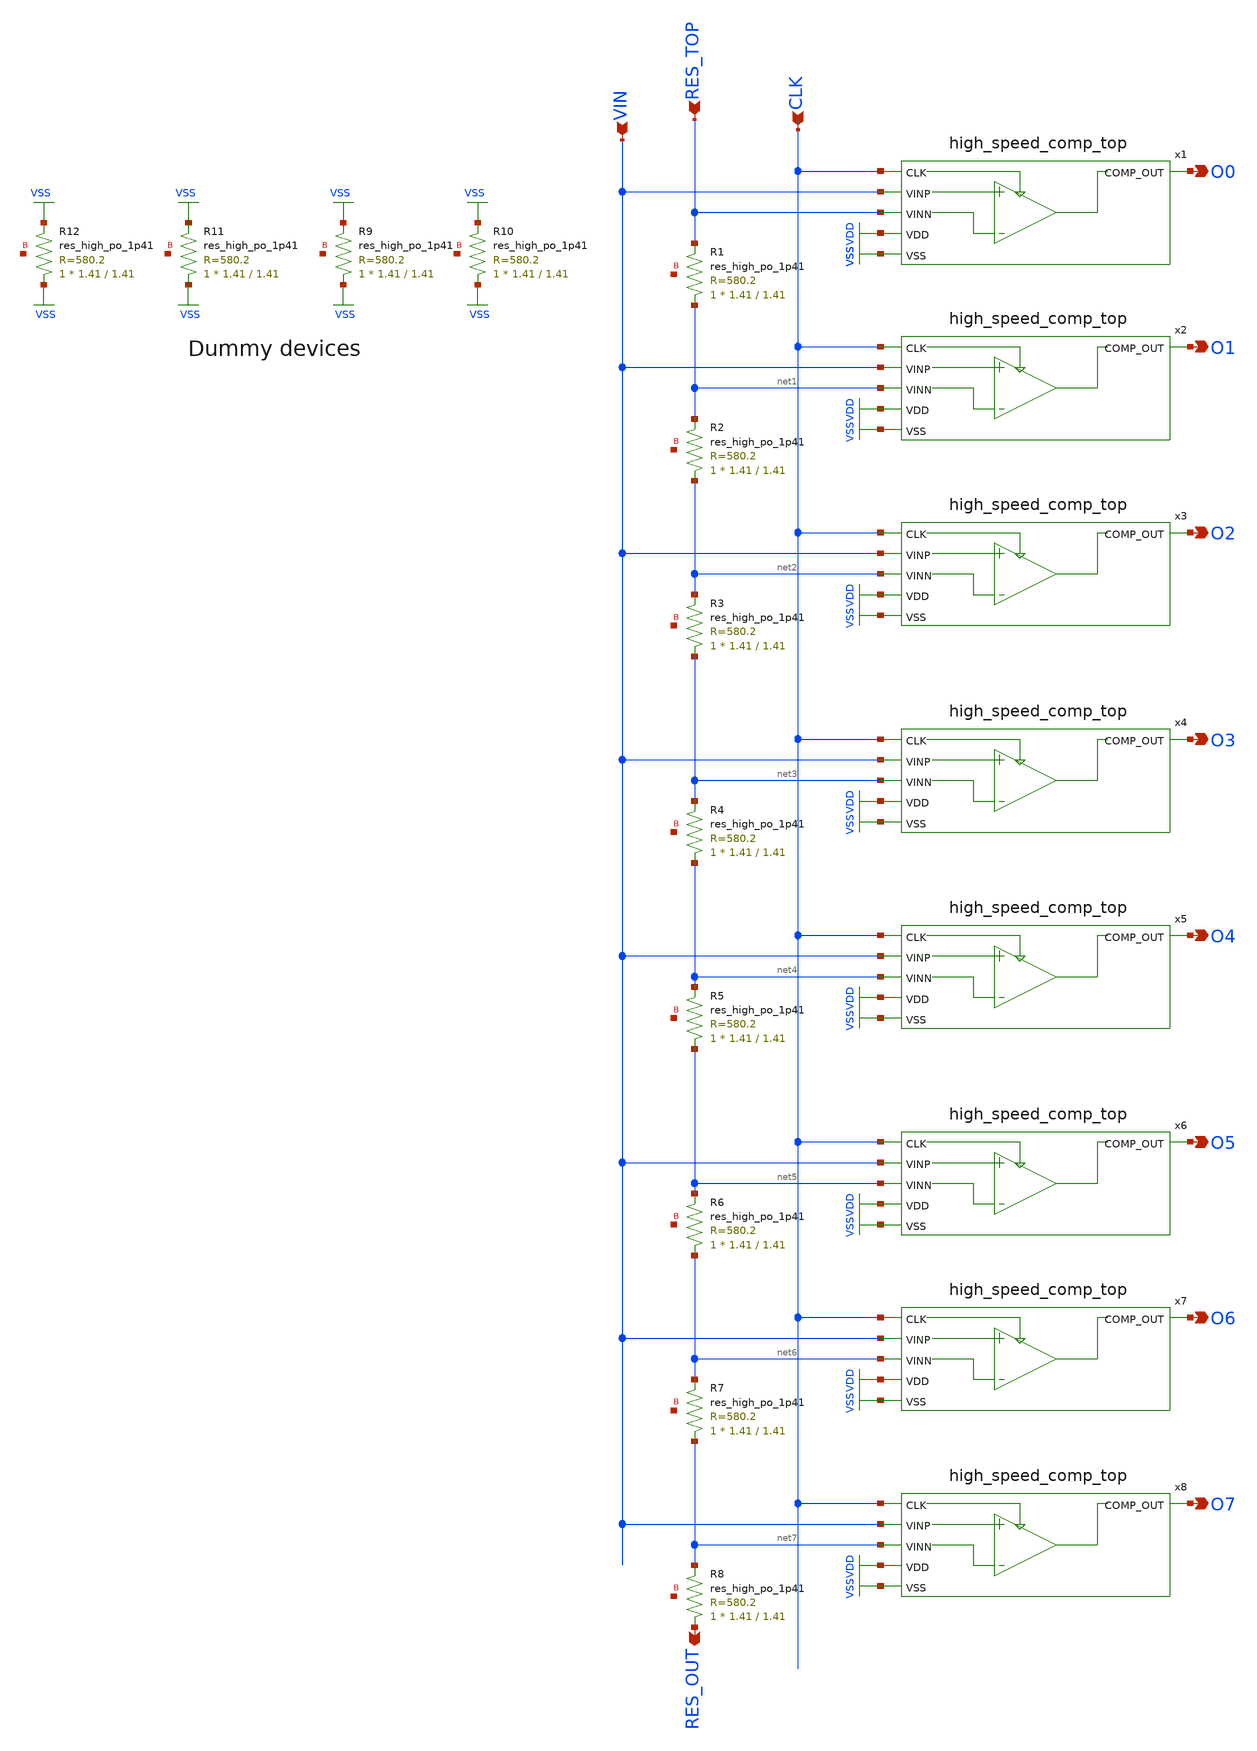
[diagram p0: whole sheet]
** sch_path: xschem/flash_converter/flash_converter.sch
**.subckt flash_converter VIN RES_TOP RES_OUT O0 O1 O2 O3 O4 O5 O6 O7 CLK
*.ipin VIN
*.ipin RES_TOP
*.opin RES_OUT
*.opin O0
*.opin O1
*.opin O2
*.opin O3
*.opin O4
*.opin O5
*.opin O6
*.opin O7
*.ipin CLK
x1 CLK VIN RES_TOP VDD O0 VSS high_speed_comp_top
x2 CLK VIN net1 VDD O1 VSS high_speed_comp_top
x3 CLK VIN net2 VDD O2 VSS high_speed_comp_top
x4 CLK VIN net3 VDD O3 VSS high_speed_comp_top
x5 CLK VIN net4 VDD O4 VSS high_speed_comp_top
x6 CLK VIN net5 VDD O5 VSS high_speed_comp_top
x7 CLK VIN net6 VDD O6 VSS high_speed_comp_top
x8 CLK VIN net7 VDD O7 VSS high_speed_comp_top
XR1 net1 RES_TOP net8 sky130_fd_pr__res_high_po_1p41 L=1.41 mult=1 m=1
XR2 net2 net1 net9 sky130_fd_pr__res_high_po_1p41 L=1.41 mult=1 m=1
XR3 net3 net2 net10 sky130_fd_pr__res_high_po_1p41 L=1.41 mult=1 m=1
XR4 net4 net3 net11 sky130_fd_pr__res_high_po_1p41 L=1.41 mult=1 m=1
XR5 net5 net4 net12 sky130_fd_pr__res_high_po_1p41 L=1.41 mult=1 m=1
XR6 net6 net5 net13 sky130_fd_pr__res_high_po_1p41 L=1.41 mult=1 m=1
XR7 net7 net6 net14 sky130_fd_pr__res_high_po_1p41 L=1.41 mult=1 m=1
XR8 RES_OUT net7 net15 sky130_fd_pr__res_high_po_1p41 L=1.41 mult=1 m=1
XR9 VSS VSS net16 sky130_fd_pr__res_high_po_1p41 L=1.41 mult=1 m=1
XR10 VSS VSS net17 sky130_fd_pr__res_high_po_1p41 L=1.41 mult=1 m=1
XR11 VSS VSS net18 sky130_fd_pr__res_high_po_1p41 L=1.41 mult=1 m=1
XR12 VSS VSS net19 sky130_fd_pr__res_high_po_1p41 L=1.41 mult=1 m=1
**.ends

* expanding   symbol:  high_speed_comp_top.sym # of pins=6
** sym_path: xschem/flash_converter/high_speed_comp_top.sym
** sch_path: xschem/flash_converter/high_speed_comp_top.sch
.subckt high_speed_comp_top CLK VINP VINN VDD COMP_OUT VSS
*.ipin VINP
*.ipin VINN
*.ipin CLK
*.opin COMP_OUT
*.ipin VDD
*.ipin VSS
x1 VDD CLK_PRIME net1 net2 VSS VINP VINN strong_arm_latch
x2 VDD net1 net2 VOUT VSS post_amplifier
x3 CLK VOUT VSS VSS VDD VDD COMP_OUT sky130_fd_sc_hd__dfxtp_2
x4 CLK VSS VSS VDD VDD CLK_PRIME sky130_fd_sc_hd__clkinv_4
x5 VSS VSS VDD VDD sky130_fd_sc_hd__decap_3
x7 VSS VSS VDD VDD sky130_fd_sc_hd__decap_3
x9 VSS VDD sky130_fd_sc_hd__tapvpwrvgnd_1
x6 VSS VDD sky130_fd_sc_hd__tapvpwrvgnd_1
x8 VSS VDD sky130_fd_sc_hd__tapvpwrvgnd_1
.ends


* expanding   symbol:  strong_arm_latch.sym # of pins=7
** sym_path: xschem/flash_converter/strong_arm_latch.sym
** sch_path: xschem/flash_converter/strong_arm_latch.sch
.subckt strong_arm_latch VDD CLK VOUT_PLUS VOUT_MINUS VSS VINP VINN
*.ipin VSS
*.ipin VDD
*.ipin CLK
*.ipin VINP
*.ipin VINN
*.opin VOUT_MINUS
*.opin VOUT_PLUS
XM1 net2 VINP net1 VSS sky130_fd_pr__nfet_01v8_lvt L=1 W=5 nf=1 ad='int((nf+1)/2) * W/nf * 0.29' as='int((nf+2)/2) * W/nf * 0.29'
+ pd='2*int((nf+1)/2) * (W/nf + 0.29)' ps='2*int((nf+2)/2) * (W/nf + 0.29)' nrd='0.29 / W' nrs='0.29 / W'
+ sa=0 sb=0 sd=0 mult=1 m=1
XM2 net3 VINN net1 VSS sky130_fd_pr__nfet_01v8_lvt L=1 W=5 nf=1 ad='int((nf+1)/2) * W/nf * 0.29' as='int((nf+2)/2) * W/nf * 0.29'
+ pd='2*int((nf+1)/2) * (W/nf + 0.29)' ps='2*int((nf+2)/2) * (W/nf + 0.29)' nrd='0.29 / W' nrs='0.29 / W'
+ sa=0 sb=0 sd=0 mult=1 m=1
XM3 net1 CLK VSS VSS sky130_fd_pr__nfet_01v8_lvt L=1 W=5 nf=1 ad='int((nf+1)/2) * W/nf * 0.29' as='int((nf+2)/2) * W/nf * 0.29'
+ pd='2*int((nf+1)/2) * (W/nf + 0.29)' ps='2*int((nf+2)/2) * (W/nf + 0.29)' nrd='0.29 / W' nrs='0.29 / W'
+ sa=0 sb=0 sd=0 mult=1 m=1
XM4 VOUT_PLUS VOUT_MINUS net2 VSS sky130_fd_pr__nfet_01v8 L=0.15 W=1 nf=1 ad='int((nf+1)/2) * W/nf * 0.29'
+ as='int((nf+2)/2) * W/nf * 0.29' pd='2*int((nf+1)/2) * (W/nf + 0.29)' ps='2*int((nf+2)/2) * (W/nf + 0.29)'
+ nrd='0.29 / W' nrs='0.29 / W' sa=0 sb=0 sd=0 mult=1 m=1
XM5 VOUT_MINUS VOUT_PLUS net3 VSS sky130_fd_pr__nfet_01v8 L=0.15 W=1 nf=1 ad='int((nf+1)/2) * W/nf * 0.29'
+ as='int((nf+2)/2) * W/nf * 0.29' pd='2*int((nf+1)/2) * (W/nf + 0.29)' ps='2*int((nf+2)/2) * (W/nf + 0.29)'
+ nrd='0.29 / W' nrs='0.29 / W' sa=0 sb=0 sd=0 mult=1 m=1
XM6 VOUT_PLUS VOUT_MINUS VDD VDD sky130_fd_pr__pfet_01v8 L=0.15 W=1 nf=1 ad='int((nf+1)/2) * W/nf * 0.29'
+ as='int((nf+2)/2) * W/nf * 0.29' pd='2*int((nf+1)/2) * (W/nf + 0.29)' ps='2*int((nf+2)/2) * (W/nf + 0.29)'
+ nrd='0.29 / W' nrs='0.29 / W' sa=0 sb=0 sd=0 mult=1 m=1
XM7 VOUT_MINUS VOUT_PLUS VDD VDD sky130_fd_pr__pfet_01v8 L=0.15 W=1 nf=1 ad='int((nf+1)/2) * W/nf * 0.29'
+ as='int((nf+2)/2) * W/nf * 0.29' pd='2*int((nf+1)/2) * (W/nf + 0.29)' ps='2*int((nf+2)/2) * (W/nf + 0.29)'
+ nrd='0.29 / W' nrs='0.29 / W' sa=0 sb=0 sd=0 mult=1 m=1
XM8 VOUT_PLUS CLK VDD VDD sky130_fd_pr__pfet_01v8 L=0.15 W=10 nf=1 ad='int((nf+1)/2) * W/nf * 0.29' as='int((nf+2)/2) * W/nf * 0.29'
+ pd='2*int((nf+1)/2) * (W/nf + 0.29)' ps='2*int((nf+2)/2) * (W/nf + 0.29)' nrd='0.29 / W' nrs='0.29 / W'
+ sa=0 sb=0 sd=0 mult=1 m=1
XM9 net2 CLK VDD VDD sky130_fd_pr__pfet_01v8 L=0.15 W=10 nf=1 ad='int((nf+1)/2) * W/nf * 0.29' as='int((nf+2)/2) * W/nf * 0.29'
+ pd='2*int((nf+1)/2) * (W/nf + 0.29)' ps='2*int((nf+2)/2) * (W/nf + 0.29)' nrd='0.29 / W' nrs='0.29 / W'
+ sa=0 sb=0 sd=0 mult=1 m=1
XM10 VOUT_MINUS CLK VDD VDD sky130_fd_pr__pfet_01v8 L=0.15 W=10 nf=1 ad='int((nf+1)/2) * W/nf * 0.29'
+ as='int((nf+2)/2) * W/nf * 0.29' pd='2*int((nf+1)/2) * (W/nf + 0.29)' ps='2*int((nf+2)/2) * (W/nf + 0.29)'
+ nrd='0.29 / W' nrs='0.29 / W' sa=0 sb=0 sd=0 mult=1 m=1
XM11 net3 CLK VDD VDD sky130_fd_pr__pfet_01v8 L=0.15 W=10 nf=1 ad='int((nf+1)/2) * W/nf * 0.29' as='int((nf+2)/2) * W/nf * 0.29'
+ pd='2*int((nf+1)/2) * (W/nf + 0.29)' ps='2*int((nf+2)/2) * (W/nf + 0.29)' nrd='0.29 / W' nrs='0.29 / W'
+ sa=0 sb=0 sd=0 mult=1 m=1
.ends


* expanding   symbol:  post_amplifier.sym # of pins=5
** sym_path: xschem/flash_converter/post_amplifier.sym
** sch_path: xschem/flash_converter/post_amplifier.sch
.subckt post_amplifier VDD VLAT_PLUS VLAT_MINUS VOUT VSS
*.ipin VLAT_PLUS
*.ipin VLAT_MINUS
*.ipin VDD
*.ipin VSS
*.opin VOUT
XM1 net1 VLAT_PLUS net4 VSS sky130_fd_pr__nfet_01v8 L=0.15 W=1 nf=1 ad='int((nf+1)/2) * W/nf * 0.29'
+ as='int((nf+2)/2) * W/nf * 0.29' pd='2*int((nf+1)/2) * (W/nf + 0.29)' ps='2*int((nf+2)/2) * (W/nf + 0.29)'
+ nrd='0.29 / W' nrs='0.29 / W' sa=0 sb=0 sd=0 mult=1 m=1
XM2 net3 VLAT_MINUS net4 VSS sky130_fd_pr__nfet_01v8 L=0.15 W=1 nf=1 ad='int((nf+1)/2) * W/nf * 0.29'
+ as='int((nf+2)/2) * W/nf * 0.29' pd='2*int((nf+1)/2) * (W/nf + 0.29)' ps='2*int((nf+2)/2) * (W/nf + 0.29)'
+ nrd='0.29 / W' nrs='0.29 / W' sa=0 sb=0 sd=0 mult=1 m=1
XM3 net4 net1 VSS VSS sky130_fd_pr__nfet_01v8 L=0.15 W=1 nf=1 ad='int((nf+1)/2) * W/nf * 0.29' as='int((nf+2)/2) * W/nf * 0.29'
+ pd='2*int((nf+1)/2) * (W/nf + 0.29)' ps='2*int((nf+2)/2) * (W/nf + 0.29)' nrd='0.29 / W' nrs='0.29 / W'
+ sa=0 sb=0 sd=0 mult=1 m=1
XM4 net1 VLAT_PLUS net2 VDD sky130_fd_pr__pfet_01v8 L=0.15 W=1 nf=1 ad='int((nf+1)/2) * W/nf * 0.29'
+ as='int((nf+2)/2) * W/nf * 0.29' pd='2*int((nf+1)/2) * (W/nf + 0.29)' ps='2*int((nf+2)/2) * (W/nf + 0.29)'
+ nrd='0.29 / W' nrs='0.29 / W' sa=0 sb=0 sd=0 mult=1 m=1
XM5 net3 VLAT_MINUS net2 VDD sky130_fd_pr__pfet_01v8 L=0.15 W=1 nf=1 ad='int((nf+1)/2) * W/nf * 0.29'
+ as='int((nf+2)/2) * W/nf * 0.29' pd='2*int((nf+1)/2) * (W/nf + 0.29)' ps='2*int((nf+2)/2) * (W/nf + 0.29)'
+ nrd='0.29 / W' nrs='0.29 / W' sa=0 sb=0 sd=0 mult=1 m=1
XM6 net2 net1 VDD VDD sky130_fd_pr__pfet_01v8 L=0.15 W=1 nf=1 ad='int((nf+1)/2) * W/nf * 0.29' as='int((nf+2)/2) * W/nf * 0.29'
+ pd='2*int((nf+1)/2) * (W/nf + 0.29)' ps='2*int((nf+2)/2) * (W/nf + 0.29)' nrd='0.29 / W' nrs='0.29 / W'
+ sa=0 sb=0 sd=0 mult=1 m=1
XM7 VOUT net3 VSS VSS sky130_fd_pr__nfet_01v8 L=0.15 W=1 nf=1 ad='int((nf+1)/2) * W/nf * 0.29' as='int((nf+2)/2) * W/nf * 0.29'
+ pd='2*int((nf+1)/2) * (W/nf + 0.29)' ps='2*int((nf+2)/2) * (W/nf + 0.29)' nrd='0.29 / W' nrs='0.29 / W'
+ sa=0 sb=0 sd=0 mult=1 m=1
XM8 VOUT net3 VDD VDD sky130_fd_pr__pfet_01v8 L=0.15 W=1 nf=1 ad='int((nf+1)/2) * W/nf * 0.29' as='int((nf+2)/2) * W/nf * 0.29'
+ pd='2*int((nf+1)/2) * (W/nf + 0.29)' ps='2*int((nf+2)/2) * (W/nf + 0.29)' nrd='0.29 / W' nrs='0.29 / W'
+ sa=0 sb=0 sd=0 mult=1 m=1
.ends

.GLOBAL VDD
.GLOBAL VSS
.end
